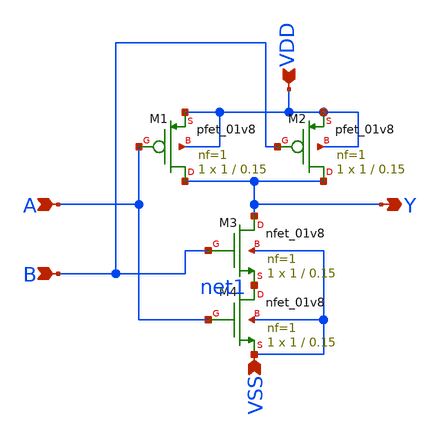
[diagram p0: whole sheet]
** sch_path: nand/design_circuit/nand.sch
**.subckt nand A B VDD VSS Y
*.ipin A
*.ipin B
*.ipin VDD
*.ipin VSS
*.opin Y
XM1 Y A VDD VDD sky130_fd_pr__pfet_01v8 L=0.15 W=1 nf=1 ad='int((nf+1)/2) * W/nf * 0.29' as='int((nf+2)/2) * W/nf * 0.29'
+ pd='2*int((nf+1)/2) * (W/nf + 0.29)' ps='2*int((nf+2)/2) * (W/nf + 0.29)' nrd='0.29 / W' nrs='0.29 / W'
+ sa=0 sb=0 sd=0 mult=1 m=1
XM2 Y B VDD VDD sky130_fd_pr__pfet_01v8 L=0.15 W=1 nf=1 ad='int((nf+1)/2) * W/nf * 0.29' as='int((nf+2)/2) * W/nf * 0.29'
+ pd='2*int((nf+1)/2) * (W/nf + 0.29)' ps='2*int((nf+2)/2) * (W/nf + 0.29)' nrd='0.29 / W' nrs='0.29 / W'
+ sa=0 sb=0 sd=0 mult=1 m=1
XM3 Y B net1 VSS sky130_fd_pr__nfet_01v8 L=0.15 W=1 nf=1 ad='int((nf+1)/2) * W/nf * 0.29' as='int((nf+2)/2) * W/nf * 0.29'
+ pd='2*int((nf+1)/2) * (W/nf + 0.29)' ps='2*int((nf+2)/2) * (W/nf + 0.29)' nrd='0.29 / W' nrs='0.29 / W'
+ sa=0 sb=0 sd=0 mult=1 m=1
XM4 net1 A VSS VSS sky130_fd_pr__nfet_01v8 L=0.15 W=1 nf=1 ad='int((nf+1)/2) * W/nf * 0.29' as='int((nf+2)/2) * W/nf * 0.29'
+ pd='2*int((nf+1)/2) * (W/nf + 0.29)' ps='2*int((nf+2)/2) * (W/nf + 0.29)' nrd='0.29 / W' nrs='0.29 / W'
+ sa=0 sb=0 sd=0 mult=1 m=1
**.ends
.end
